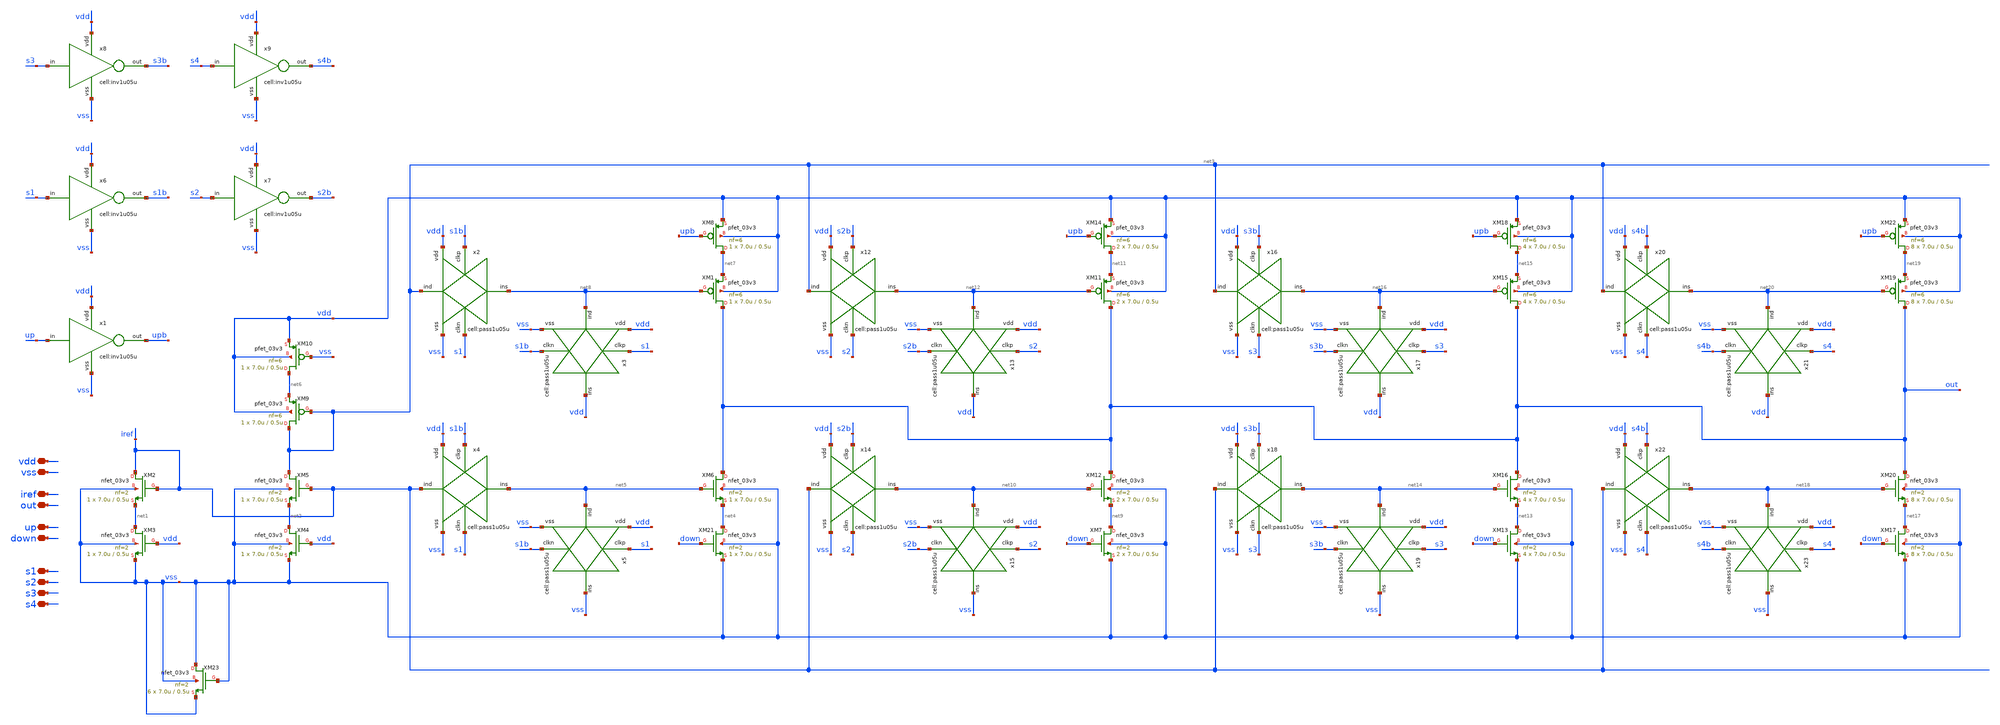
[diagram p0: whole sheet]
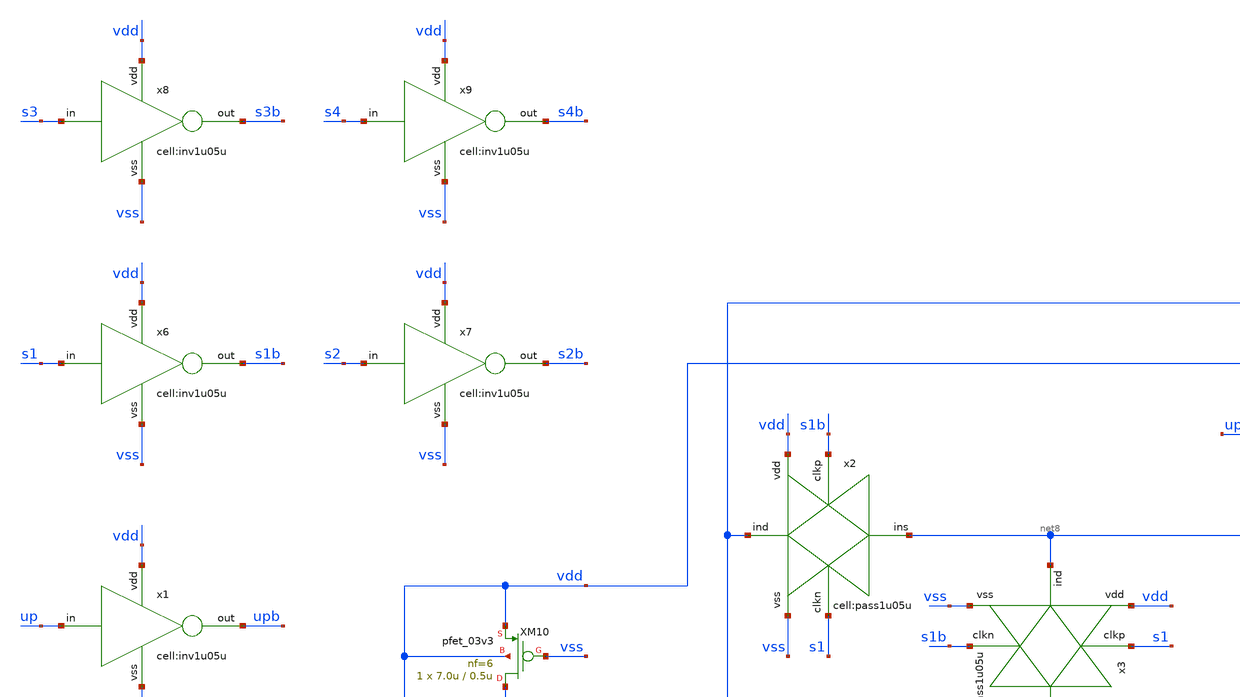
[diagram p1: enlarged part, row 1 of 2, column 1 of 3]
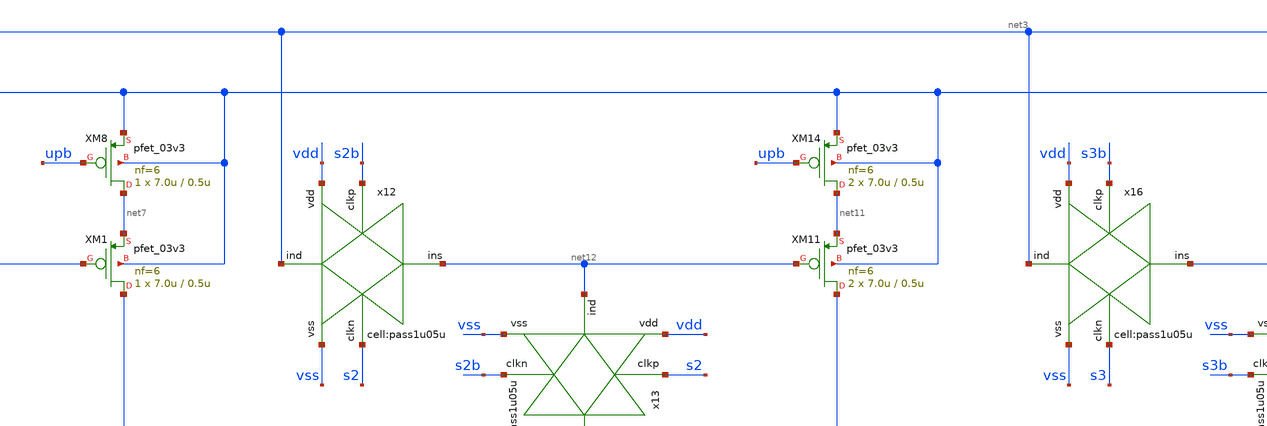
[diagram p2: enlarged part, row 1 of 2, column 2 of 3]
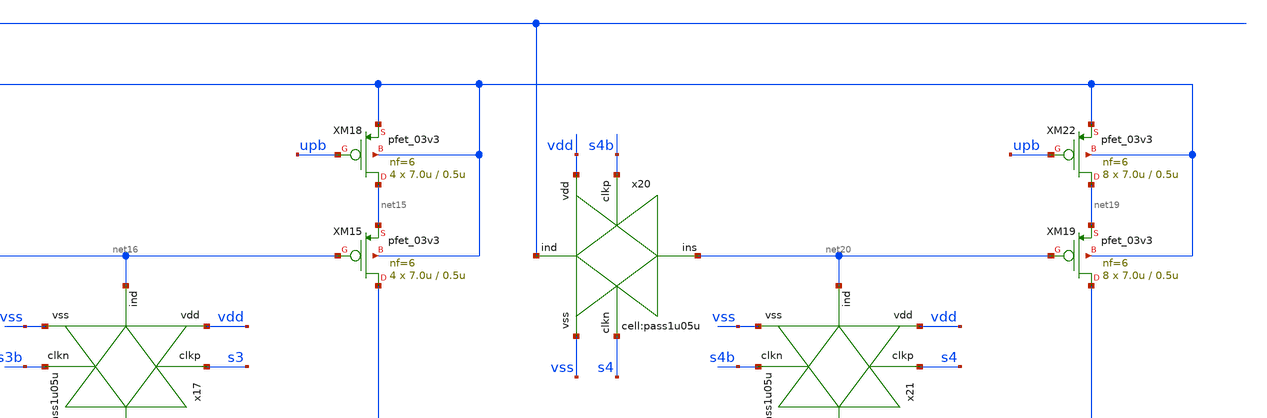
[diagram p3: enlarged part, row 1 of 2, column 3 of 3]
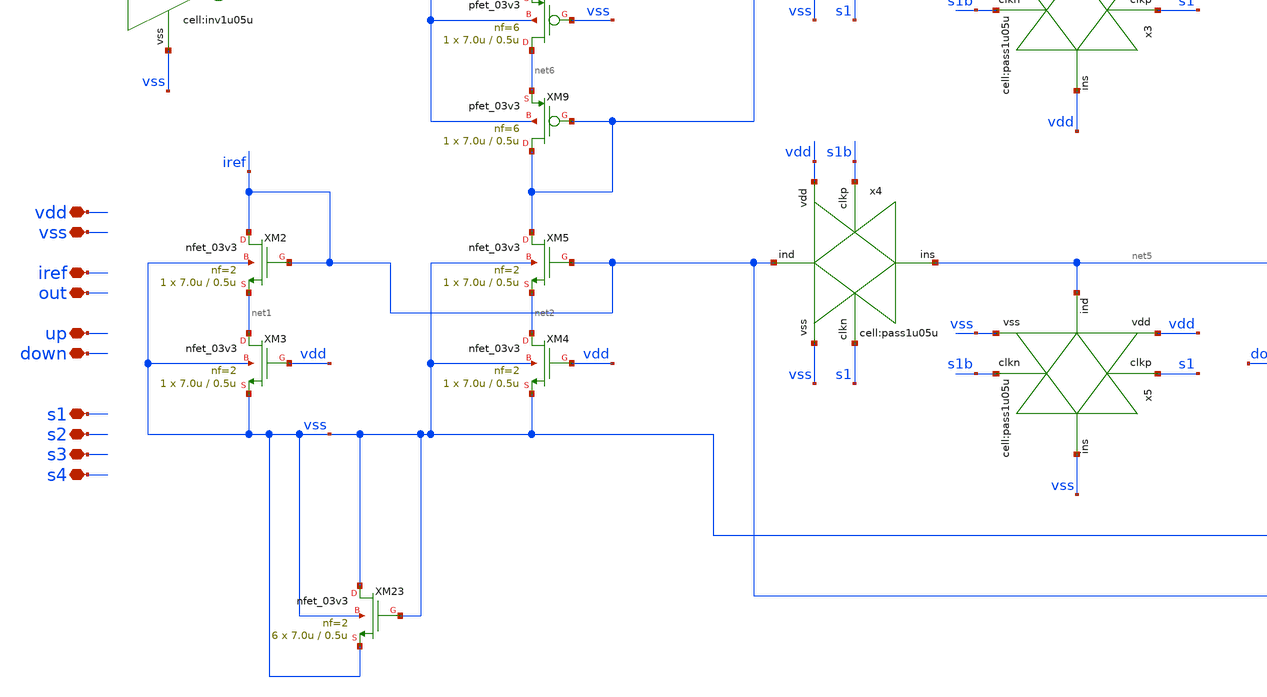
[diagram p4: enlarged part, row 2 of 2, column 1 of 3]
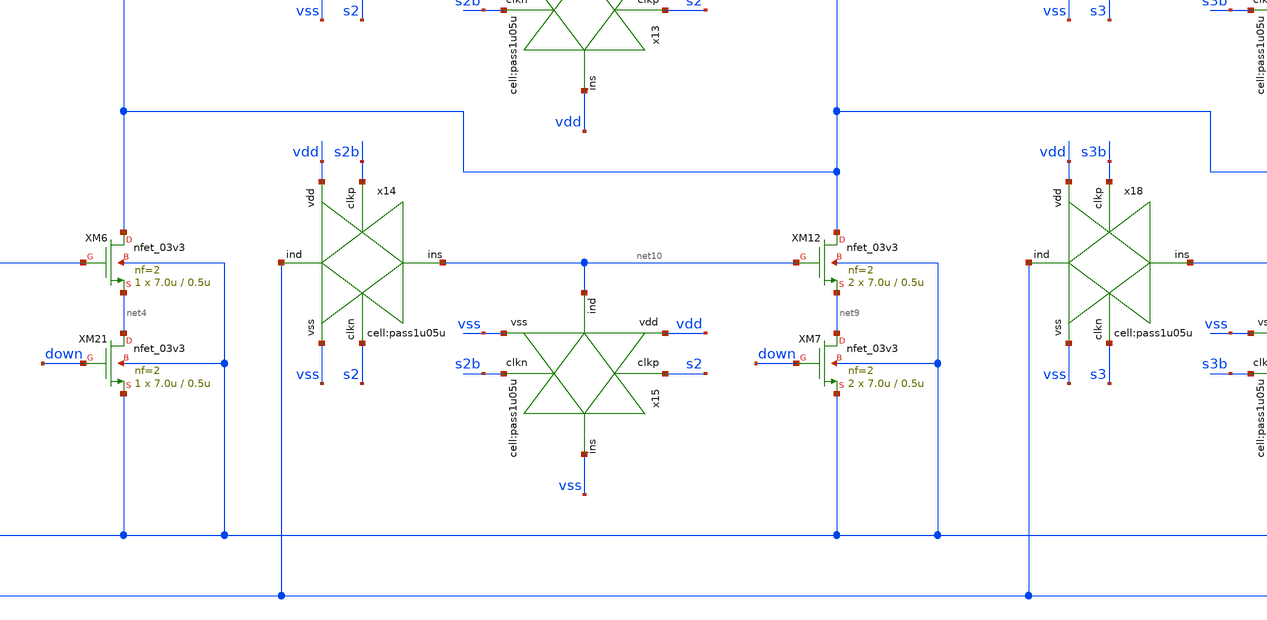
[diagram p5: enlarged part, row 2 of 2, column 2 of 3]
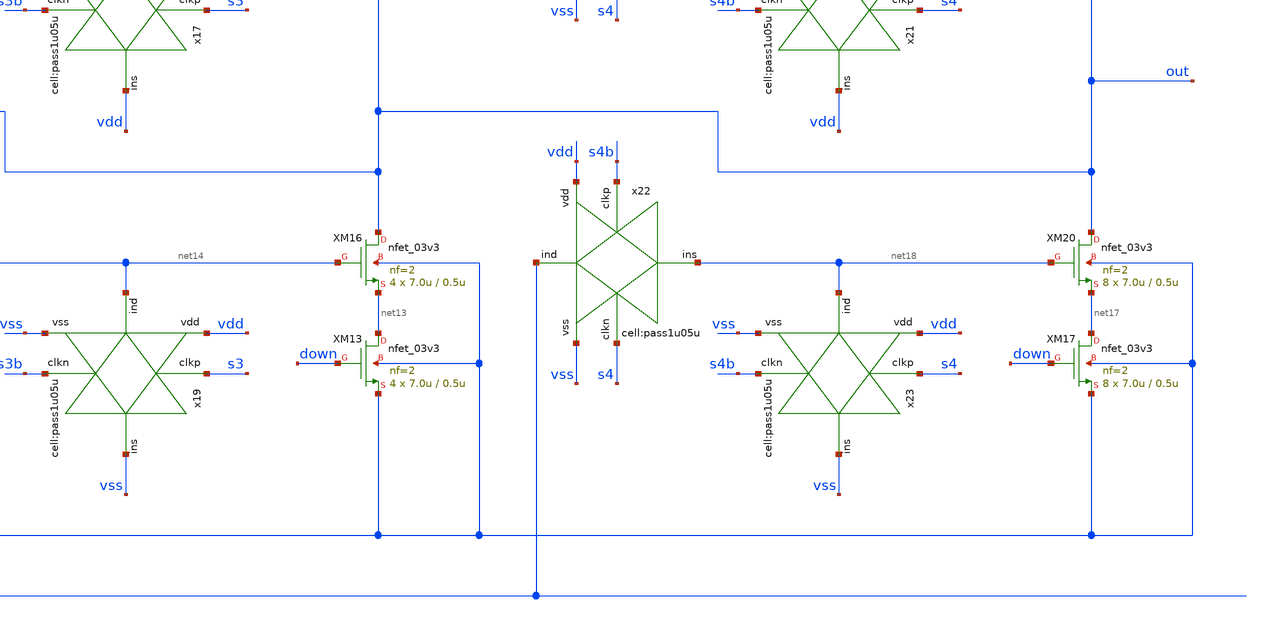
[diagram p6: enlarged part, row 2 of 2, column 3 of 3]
** sch_path: designs/libs/xp_core_analog/xp_programmable_basic_pump/xp_programmable_basic_pump.sch
**.subckt xp_programmable_basic_pump vdd vss up down iref out s3 s4 s1 s2
*.iopin vdd
*.iopin vss
*.iopin up
*.iopin down
*.iopin iref
*.iopin out
*.iopin s3
*.iopin s4
*.iopin s1
*.iopin s2
XM6 out net5 net4 vss nfet_03v3 L=0.5u W=7.0u nf=2 ad='int((nf+1)/2) * W/nf * 0.18u' as='int((nf+2)/2) * W/nf * 0.18u'
+ pd='2*int((nf+1)/2) * (W/nf + 0.18u)' ps='2*int((nf+2)/2) * (W/nf + 0.18u)' nrd='0.18u / W' nrs='0.18u / W'
+ sa=0 sb=0 sd=0 m=1
XM8 net7 upb vdd vdd pfet_03v3 L=0.5u W=7.0u nf=6 ad='int((nf+1)/2) * W/nf * 0.18u' as='int((nf+2)/2) * W/nf * 0.18u'
+ pd='2*int((nf+1)/2) * (W/nf + 0.18u)' ps='2*int((nf+2)/2) * (W/nf + 0.18u)' nrd='0.18u / W' nrs='0.18u / W'
+ sa=0 sb=0 sd=0 m=1
XM10 net6 vss vdd vdd pfet_03v3 L=0.5u W=7.0u nf=6 ad='int((nf+1)/2) * W/nf * 0.18u' as='int((nf+2)/2) * W/nf * 0.18u'
+ pd='2*int((nf+1)/2) * (W/nf + 0.18u)' ps='2*int((nf+2)/2) * (W/nf + 0.18u)' nrd='0.18u / W' nrs='0.18u / W'
+ sa=0 sb=0 sd=0 m=1
x1 up vdd upb vss inv1u05u
x2 net3 vss s1 net8 s1b vdd pass1u05u
x3 net8 vss s1b vdd s1 vdd pass1u05u
x4 iref vss s1 net5 s1b vdd pass1u05u
x5 net5 vss s1b vss s1 vdd pass1u05u
x6 s1 vdd s1b vss inv1u05u
x7 s2 vdd s2b vss inv1u05u
x8 s3 vdd s3b vss inv1u05u
x9 s4 vdd s4b vss inv1u05u
XM12 out net10 net9 vss nfet_03v3 L=0.5u W=7.0u nf=2 ad='int((nf+1)/2) * W/nf * 0.18u' as='int((nf+2)/2) * W/nf * 0.18u'
+ pd='2*int((nf+1)/2) * (W/nf + 0.18u)' ps='2*int((nf+2)/2) * (W/nf + 0.18u)' nrd='0.18u / W' nrs='0.18u / W'
+ sa=0 sb=0 sd=0 m=2
XM14 net11 upb vdd vdd pfet_03v3 L=0.5u W=7.0u nf=6 ad='int((nf+1)/2) * W/nf * 0.18u' as='int((nf+2)/2) * W/nf * 0.18u'
+ pd='2*int((nf+1)/2) * (W/nf + 0.18u)' ps='2*int((nf+2)/2) * (W/nf + 0.18u)' nrd='0.18u / W' nrs='0.18u / W'
+ sa=0 sb=0 sd=0 m=2
x12 net3 vss s2 net12 s2b vdd pass1u05u
x13 net12 vss s2b vdd s2 vdd pass1u05u
x14 iref vss s2 net10 s2b vdd pass1u05u
x15 net10 vss s2b vss s2 vdd pass1u05u
XM16 out net14 net13 vss nfet_03v3 L=0.5u W=7.0u nf=2 ad='int((nf+1)/2) * W/nf * 0.18u' as='int((nf+2)/2) * W/nf * 0.18u'
+ pd='2*int((nf+1)/2) * (W/nf + 0.18u)' ps='2*int((nf+2)/2) * (W/nf + 0.18u)' nrd='0.18u / W' nrs='0.18u / W'
+ sa=0 sb=0 sd=0 m=4
XM18 net15 upb vdd vdd pfet_03v3 L=0.5u W=7.0u nf=6 ad='int((nf+1)/2) * W/nf * 0.18u' as='int((nf+2)/2) * W/nf * 0.18u'
+ pd='2*int((nf+1)/2) * (W/nf + 0.18u)' ps='2*int((nf+2)/2) * (W/nf + 0.18u)' nrd='0.18u / W' nrs='0.18u / W'
+ sa=0 sb=0 sd=0 m=4
x16 net3 vss s3 net16 s3b vdd pass1u05u
x17 net16 vss s3b vdd s3 vdd pass1u05u
x18 iref vss s3 net14 s3b vdd pass1u05u
x19 net14 vss s3b vss s3 vdd pass1u05u
XM19 out net20 net19 vdd pfet_03v3 L=0.5u W=7.0u nf=6 ad='int((nf+1)/2) * W/nf * 0.18u' as='int((nf+2)/2) * W/nf * 0.18u'
+ pd='2*int((nf+1)/2) * (W/nf + 0.18u)' ps='2*int((nf+2)/2) * (W/nf + 0.18u)' nrd='0.18u / W' nrs='0.18u / W'
+ sa=0 sb=0 sd=0 m=8
XM20 out net18 net17 vss nfet_03v3 L=0.5u W=7.0u nf=2 ad='int((nf+1)/2) * W/nf * 0.18u' as='int((nf+2)/2) * W/nf * 0.18u'
+ pd='2*int((nf+1)/2) * (W/nf + 0.18u)' ps='2*int((nf+2)/2) * (W/nf + 0.18u)' nrd='0.18u / W' nrs='0.18u / W'
+ sa=0 sb=0 sd=0 m=8
XM22 net19 upb vdd vdd pfet_03v3 L=0.5u W=7.0u nf=6 ad='int((nf+1)/2) * W/nf * 0.18u' as='int((nf+2)/2) * W/nf * 0.18u'
+ pd='2*int((nf+1)/2) * (W/nf + 0.18u)' ps='2*int((nf+2)/2) * (W/nf + 0.18u)' nrd='0.18u / W' nrs='0.18u / W'
+ sa=0 sb=0 sd=0 m=8
x20 net3 vss s4 net20 s4b vdd pass1u05u
x21 net20 vss s4b vdd s4 vdd pass1u05u
x22 iref vss s4 net18 s4b vdd pass1u05u
x23 net18 vss s4b vss s4 vdd pass1u05u
XM2 iref iref net1 vss nfet_03v3 L=0.5u W=7.0u nf=2 ad='int((nf+1)/2) * W/nf * 0.18u' as='int((nf+2)/2) * W/nf * 0.18u'
+ pd='2*int((nf+1)/2) * (W/nf + 0.18u)' ps='2*int((nf+2)/2) * (W/nf + 0.18u)' nrd='0.18u / W' nrs='0.18u / W'
+ sa=0 sb=0 sd=0 m=1
XM9 net3 net3 net6 vdd pfet_03v3 L=0.5u W=7.0u nf=6 ad='int((nf+1)/2) * W/nf * 0.18u' as='int((nf+2)/2) * W/nf * 0.18u'
+ pd='2*int((nf+1)/2) * (W/nf + 0.18u)' ps='2*int((nf+2)/2) * (W/nf + 0.18u)' nrd='0.18u / W' nrs='0.18u / W'
+ sa=0 sb=0 sd=0 m=1
XM1 out net8 net7 vdd pfet_03v3 L=0.5u W=7.0u nf=6 ad='int((nf+1)/2) * W/nf * 0.18u' as='int((nf+2)/2) * W/nf * 0.18u'
+ pd='2*int((nf+1)/2) * (W/nf + 0.18u)' ps='2*int((nf+2)/2) * (W/nf + 0.18u)' nrd='0.18u / W' nrs='0.18u / W'
+ sa=0 sb=0 sd=0 m=1
XM11 out net12 net11 vdd pfet_03v3 L=0.5u W=7.0u nf=6 ad='int((nf+1)/2) * W/nf * 0.18u' as='int((nf+2)/2) * W/nf * 0.18u'
+ pd='2*int((nf+1)/2) * (W/nf + 0.18u)' ps='2*int((nf+2)/2) * (W/nf + 0.18u)' nrd='0.18u / W' nrs='0.18u / W'
+ sa=0 sb=0 sd=0 m=2
XM15 out net16 net15 vdd pfet_03v3 L=0.5u W=7.0u nf=6 ad='int((nf+1)/2) * W/nf * 0.18u' as='int((nf+2)/2) * W/nf * 0.18u'
+ pd='2*int((nf+1)/2) * (W/nf + 0.18u)' ps='2*int((nf+2)/2) * (W/nf + 0.18u)' nrd='0.18u / W' nrs='0.18u / W'
+ sa=0 sb=0 sd=0 m=4
XM3 net1 vdd vss vss nfet_03v3 L=0.5u W=7.0u nf=2 ad='int((nf+1)/2) * W/nf * 0.18u' as='int((nf+2)/2) * W/nf * 0.18u'
+ pd='2*int((nf+1)/2) * (W/nf + 0.18u)' ps='2*int((nf+2)/2) * (W/nf + 0.18u)' nrd='0.18u / W' nrs='0.18u / W'
+ sa=0 sb=0 sd=0 m=1
XM4 net2 vdd vss vss nfet_03v3 L=0.5u W=7.0u nf=2 ad='int((nf+1)/2) * W/nf * 0.18u' as='int((nf+2)/2) * W/nf * 0.18u'
+ pd='2*int((nf+1)/2) * (W/nf + 0.18u)' ps='2*int((nf+2)/2) * (W/nf + 0.18u)' nrd='0.18u / W' nrs='0.18u / W'
+ sa=0 sb=0 sd=0 m=1
XM5 net3 iref net2 vss nfet_03v3 L=0.5u W=7.0u nf=2 ad='int((nf+1)/2) * W/nf * 0.18u' as='int((nf+2)/2) * W/nf * 0.18u'
+ pd='2*int((nf+1)/2) * (W/nf + 0.18u)' ps='2*int((nf+2)/2) * (W/nf + 0.18u)' nrd='0.18u / W' nrs='0.18u / W'
+ sa=0 sb=0 sd=0 m=1
XM21 net4 down vss vss nfet_03v3 L=0.5u W=7.0u nf=2 ad='int((nf+1)/2) * W/nf * 0.18u' as='int((nf+2)/2) * W/nf * 0.18u'
+ pd='2*int((nf+1)/2) * (W/nf + 0.18u)' ps='2*int((nf+2)/2) * (W/nf + 0.18u)' nrd='0.18u / W' nrs='0.18u / W'
+ sa=0 sb=0 sd=0 m=1
XM7 net9 down vss vss nfet_03v3 L=0.5u W=7.0u nf=2 ad='int((nf+1)/2) * W/nf * 0.18u' as='int((nf+2)/2) * W/nf * 0.18u'
+ pd='2*int((nf+1)/2) * (W/nf + 0.18u)' ps='2*int((nf+2)/2) * (W/nf + 0.18u)' nrd='0.18u / W' nrs='0.18u / W'
+ sa=0 sb=0 sd=0 m=2
XM13 net13 down vss vss nfet_03v3 L=0.5u W=7.0u nf=2 ad='int((nf+1)/2) * W/nf * 0.18u' as='int((nf+2)/2) * W/nf * 0.18u'
+ pd='2*int((nf+1)/2) * (W/nf + 0.18u)' ps='2*int((nf+2)/2) * (W/nf + 0.18u)' nrd='0.18u / W' nrs='0.18u / W'
+ sa=0 sb=0 sd=0 m=4
XM17 net17 down vss vss nfet_03v3 L=0.5u W=7.0u nf=2 ad='int((nf+1)/2) * W/nf * 0.18u' as='int((nf+2)/2) * W/nf * 0.18u'
+ pd='2*int((nf+1)/2) * (W/nf + 0.18u)' ps='2*int((nf+2)/2) * (W/nf + 0.18u)' nrd='0.18u / W' nrs='0.18u / W'
+ sa=0 sb=0 sd=0 m=8
XM23 vss vss vss vss nfet_03v3 L=0.5u W=7.0u nf=2 ad='int((nf+1)/2) * W/nf * 0.18u' as='int((nf+2)/2) * W/nf * 0.18u'
+ pd='2*int((nf+1)/2) * (W/nf + 0.18u)' ps='2*int((nf+2)/2) * (W/nf + 0.18u)' nrd='0.18u / W' nrs='0.18u / W'
+ sa=0 sb=0 sd=0 m=6
**.ends
.end
